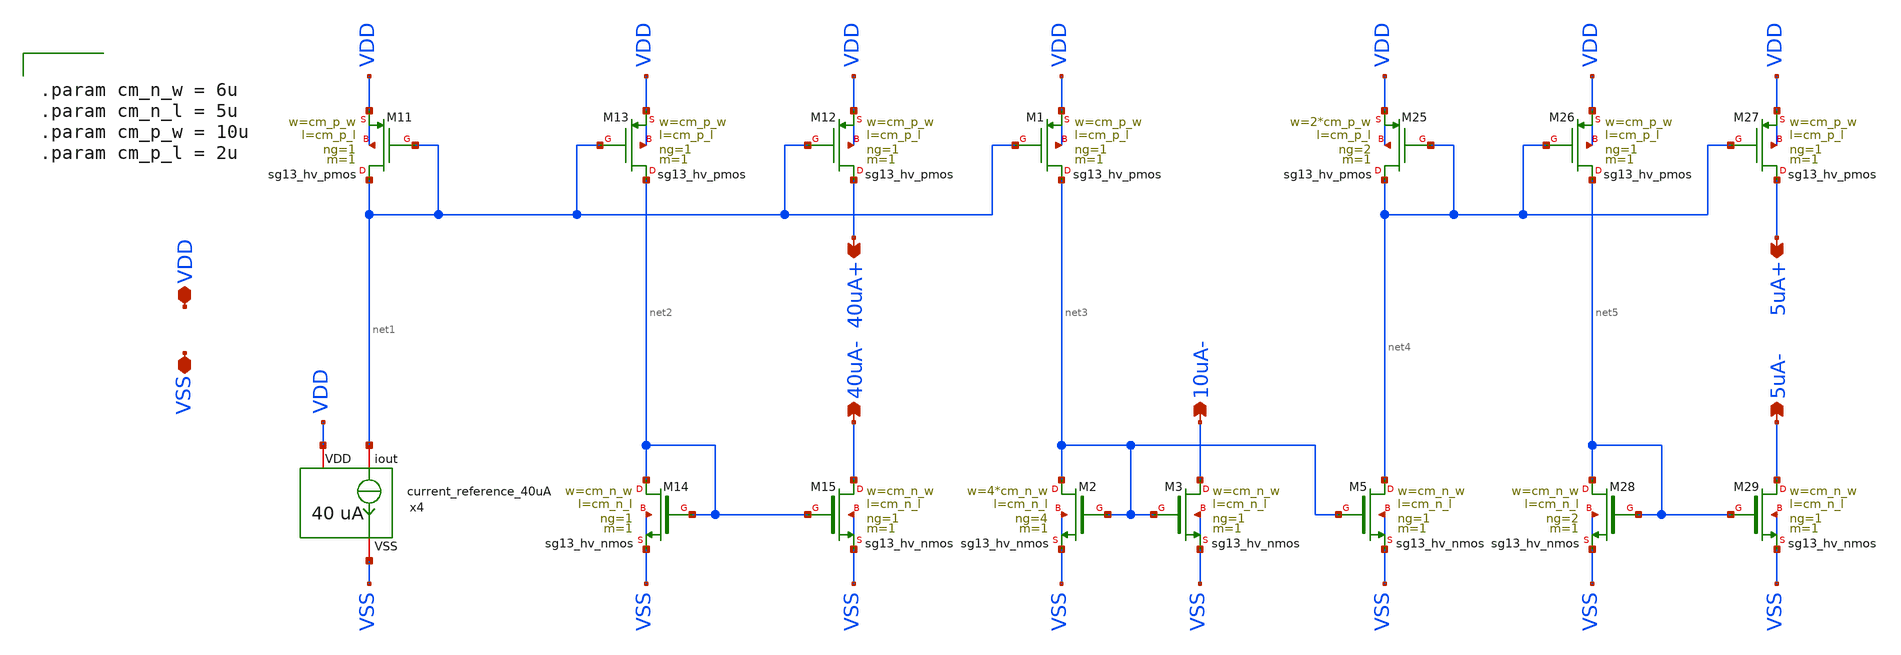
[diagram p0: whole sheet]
** sch_path: macros/heichips26_vcr/macros/switched_capacitor/schematic/xschem/bias_current_generator.sch
**.subckt bias_current_generator 40uA+ VSS VDD 40uA- 10uA- 5uA+ 5uA-
*.opin 40uA+
*.iopin VSS
*.iopin VDD
*.opin 40uA-
*.opin 10uA-
*.opin 5uA+
*.opin 5uA-
x4 VDD net1 VSS current_reference_40uA
XM11 net1 net1 VDD VDD sg13_hv_pmos w=cm_p_w l=cm_p_l ng=1 m=1 mm_ok=1
XM12 40uA+ net1 VDD VDD sg13_hv_pmos w=cm_p_w l=cm_p_l ng=1 m=1 mm_ok=1
XM13 net2 net1 VDD VDD sg13_hv_pmos w=cm_p_w l=cm_p_l ng=1 m=1 mm_ok=1
XM14 net2 net2 VSS VSS sg13_hv_nmos w=cm_n_w l=cm_n_l ng=1 m=1 mm_ok=1
XM15 40uA- net2 VSS VSS sg13_hv_nmos w=cm_n_w l=cm_n_l ng=1 m=1 mm_ok=1
XM1 net3 net1 VDD VDD sg13_hv_pmos w=cm_p_w l=cm_p_l ng=1 m=1 mm_ok=1
XM2 net3 net3 VSS VSS sg13_hv_nmos w=4*cm_n_w l=cm_n_l ng=4 m=1 mm_ok=1
XM3 10uA- net3 VSS VSS sg13_hv_nmos w=cm_n_w l=cm_n_l ng=1 m=1 mm_ok=1
XM5 net4 net3 VSS VSS sg13_hv_nmos w=cm_n_w l=cm_n_l ng=1 m=1 mm_ok=1
XM25 net4 net4 VDD VDD sg13_hv_pmos w=2*cm_p_w l=cm_p_l ng=2 m=1 mm_ok=1
XM26 net5 net4 VDD VDD sg13_hv_pmos w=cm_p_w l=cm_p_l ng=1 m=1 mm_ok=1
XM27 5uA+ net4 VDD VDD sg13_hv_pmos w=cm_p_w l=cm_p_l ng=1 m=1 mm_ok=1
XM28 net5 net5 VSS VSS sg13_hv_nmos w=cm_n_w l=cm_n_l ng=2 m=1 mm_ok=1
XM29 5uA- net5 VSS VSS sg13_hv_nmos w=cm_n_w l=cm_n_l ng=1 m=1 mm_ok=1
**** begin user architecture code


.param cm_n_w = 6u
.param cm_n_l = 5u
.param cm_p_w = 10u
.param cm_p_l = 2u


**** end user architecture code
**.ends

* expanding   symbol:  current_reference_40uA.sym # of pins=3
** sym_path: macros/heichips26_vcr/macros/switched_capacitor/schematic/xschem/current_reference_40uA.sym
** sch_path: macros/heichips26_vcr/macros/switched_capacitor/schematic/xschem/current_reference_40uA.sch
.subckt current_reference_40uA VDD iout VSS
*.iopin VSS
*.iopin VDD
*.iopin iout
XM8 net2 net2 VSS VSS sg13_hv_nmos w=n_w l=n_l ng=1 m=1 mm_ok=1
XM6 net2 net1 VDD VDD sg13_hv_pmos w=p_w l=p_l ng=1 m=1 mm_ok=1
XM1 net1 net1 VDD VDD sg13_hv_pmos w=p_w l=p_l ng=1 m=1 mm_ok=1
XM3 net1 net2 net3 VSS sg13_hv_nmos w=n_w l=n_l ng=1 m=1 mm_ok=1
XR2 net4 VSS VSS rppd w=2e-6 l=21.9e-6 m=1 b=0 mm_ok=1
XM2 net1 net2 net3 VSS sg13_hv_nmos w=n_w l=n_l ng=1 m=1 mm_ok=1
XM4 net1 net2 net3 VSS sg13_hv_nmos w=n_w l=n_l ng=1 m=1 mm_ok=1
XM5 net1 net2 net3 VSS sg13_hv_nmos w=n_w l=n_l ng=1 m=1 mm_ok=1
XM7 iout net2 VSS VSS sg13_hv_nmos w=n_w l=n_l ng=1 m=1 mm_ok=1
XR3 net3 net4 VSS rsil w=0.5e-6 l=365e-6 m=1 mm_ok=1
**** begin user architecture code


.param n_w = 6u
.param n_l = 5u
.param p_w = 10u
.param p_l = 2u


**** end user architecture code
.ends

.end
